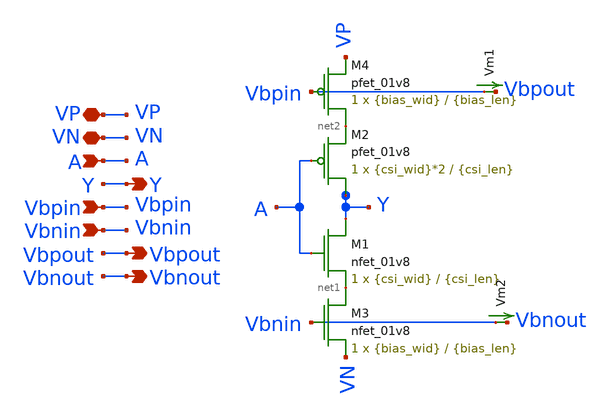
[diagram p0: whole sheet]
** sch_path: csi.sch
**.subckt csi VN VP Y Vbpin A Vbnin Vbpout Vbnout
*.iopin VN
*.iopin VP
*.opin Y
*.ipin Vbpin
*.ipin A
*.ipin Vbnin
*.opin Vbpout
*.opin Vbnout
XM1 Y A net1 VN sky130_fd_pr__nfet_01v8 L={csi_len} W={csi_wid} nf=1 ad='int((nf+1)/2) * W/nf * 0.29'
+ as='int((nf+2)/2) * W/nf * 0.29' pd='2*int((nf+1)/2) * (W/nf + 0.29)' ps='2*int((nf+2)/2) * (W/nf + 0.29)'
+ nrd='0.29 / W' nrs='0.29 / W' sa=0 sb=0 sd=0 mult=1 m=1
XM2 Y A net2 VP sky130_fd_pr__pfet_01v8 L={csi_len} W={csi_wid}*2 nf=1 ad='int((nf+1)/2) * W/nf * 0.29'
+ as='int((nf+2)/2) * W/nf * 0.29' pd='2*int((nf+1)/2) * (W/nf + 0.29)' ps='2*int((nf+2)/2) * (W/nf + 0.29)'
+ nrd='0.29 / W' nrs='0.29 / W' sa=0 sb=0 sd=0 mult=1 m=1
XM3 net1 Vbnin VN VN sky130_fd_pr__nfet_01v8 L={bias_len} W={bias_wid} nf=1 ad='int((nf+1)/2) * W/nf * 0.29'
+ as='int((nf+2)/2) * W/nf * 0.29' pd='2*int((nf+1)/2) * (W/nf + 0.29)' ps='2*int((nf+2)/2) * (W/nf + 0.29)'
+ nrd='0.29 / W' nrs='0.29 / W' sa=0 sb=0 sd=0 mult=1 m=1
XM4 net2 Vbpin VP VP sky130_fd_pr__pfet_01v8 L={bias_len} W={bias_wid} nf=1 ad='int((nf+1)/2) * W/nf * 0.29'
+ as='int((nf+2)/2) * W/nf * 0.29' pd='2*int((nf+1)/2) * (W/nf + 0.29)' ps='2*int((nf+2)/2) * (W/nf + 0.29)'
+ nrd='0.29 / W' nrs='0.29 / W' sa=0 sb=0 sd=0 mult=1 m=1
Vm1 Vbpin Vbpout 0
.save i(vm1)
Vm2 Vbnin Vbnout 0
.save i(vm2)
**.ends
.end
